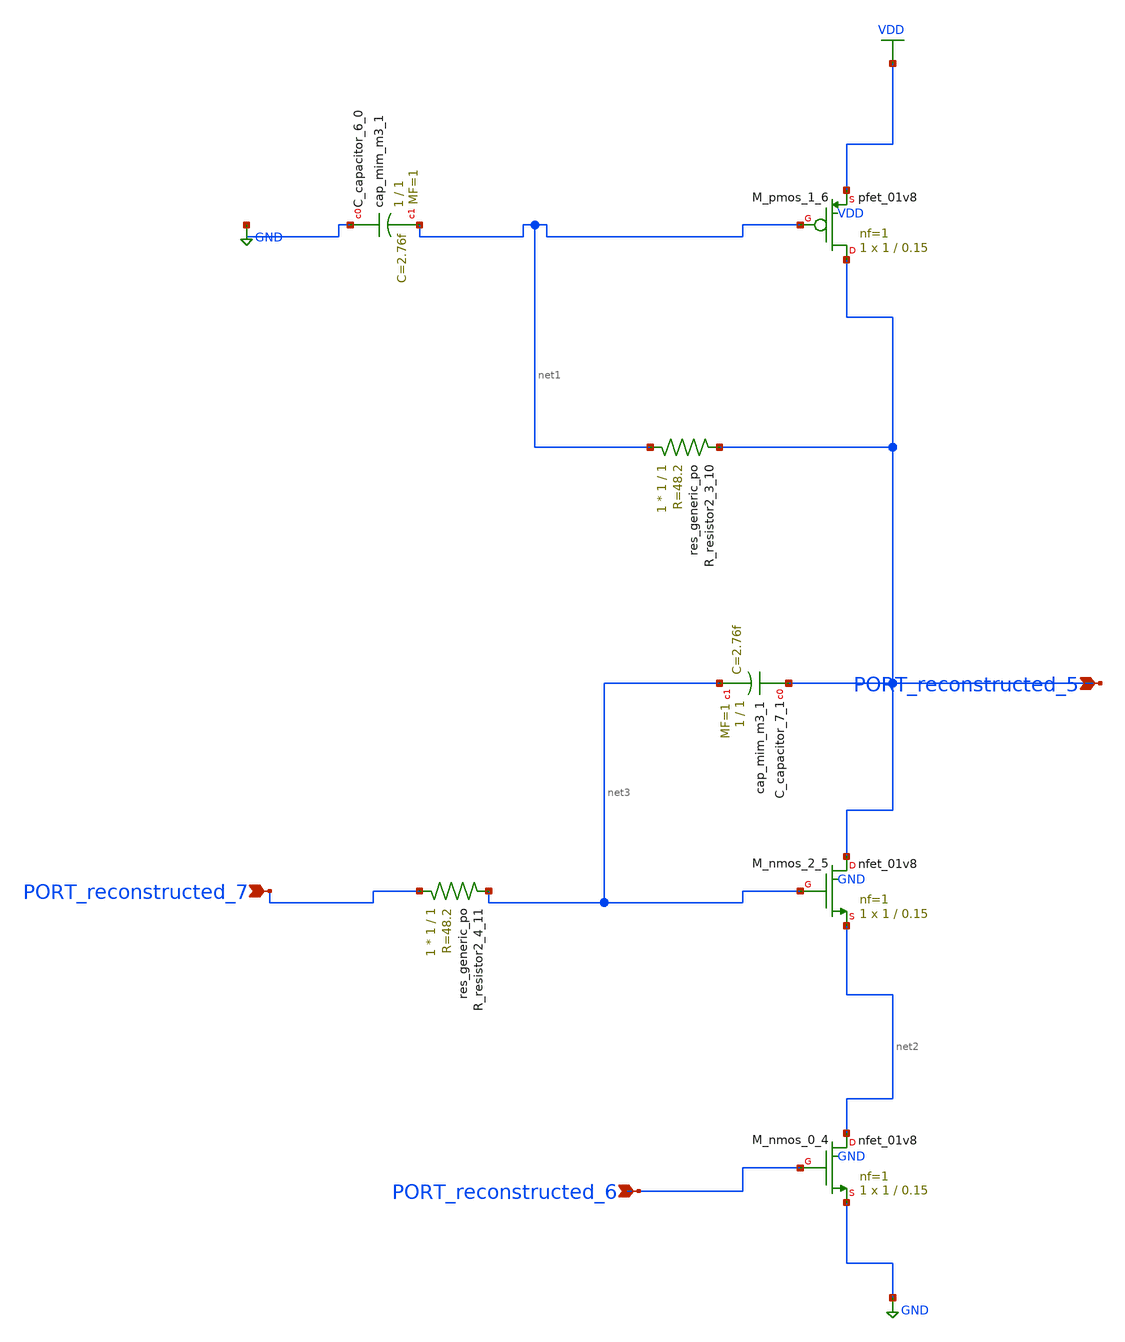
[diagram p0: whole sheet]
** sch_path: schematics/AMSNet/419.sch
**.subckt 419 PORT_reconstructed_6 PORT_reconstructed_7 PORT_reconstructed_5
*.ipin PORT_reconstructed_6
*.ipin PORT_reconstructed_7
*.ipin PORT_reconstructed_5
XC_capacitor_6_0 GND net1 sky130_fd_pr__cap_mim_m3_1 W=1 L=1 MF=1 m=1
XC_capacitor_7_1 PORT_reconstructed_5 net3 sky130_fd_pr__cap_mim_m3_1 W=1 L=1 MF=1 m=1
XM_nmos_0_4 net2 PORT_reconstructed_6 GND GND sky130_fd_pr__nfet_01v8 L=0.15 W=1 nf=1 ad='int((1 + 1)/2) * 1 / 1 * 0.29'
+ as='int((1 + 2)/2) * 1 / 1 * 0.29' pd='2*int((1 + 1)/2) * (1 / 1 + 0.29)' ps='2*int((1 + 2)/2) * (1 / 1 + 0.29)'
+ nrd='0.29 / 1 ' nrs='0.29 / 1 ' sa=0 sb=0 sd=0 mult=1 m=1
XM_nmos_2_5 PORT_reconstructed_5 net3 net2 GND sky130_fd_pr__nfet_01v8 L=0.15 W=1 nf=1 ad='int((1 + 1)/2) * 1 / 1 * 0.29'
+ as='int((1 + 2)/2) * 1 / 1 * 0.29' pd='2*int((1 + 1)/2) * (1 / 1 + 0.29)' ps='2*int((1 + 2)/2) * (1 / 1 + 0.29)'
+ nrd='0.29 / 1 ' nrs='0.29 / 1 ' sa=0 sb=0 sd=0 mult=1 m=1
XM_pmos_1_6 PORT_reconstructed_5 net1 VDD VDD sky130_fd_pr__pfet_01v8 L=0.15 W=1 nf=1 ad='int((1 + 1)/2) * 1 / 1 * 0.29'
+ as='int((1 + 2)/2) * 1 / 1 * 0.29' pd='2*int((1 + 1)/2) * (1 / 1 + 0.29)' ps='2*int((1 + 2)/2) * (1 / 1 + 0.29)'
+ nrd='0.29 / 1 ' nrs='0.29 / 1 ' sa=0 sb=0 sd=0 mult=1 m=1
XR_resistor2_3_10 net1 PORT_reconstructed_5 sky130_fd_pr__res_generic_po W=1 L=1 m=1
XR_resistor2_4_11 PORT_reconstructed_7 net3 sky130_fd_pr__res_generic_po W=1 L=1 m=1
**.ends
.GLOBAL GND
.GLOBAL VDD
.end
